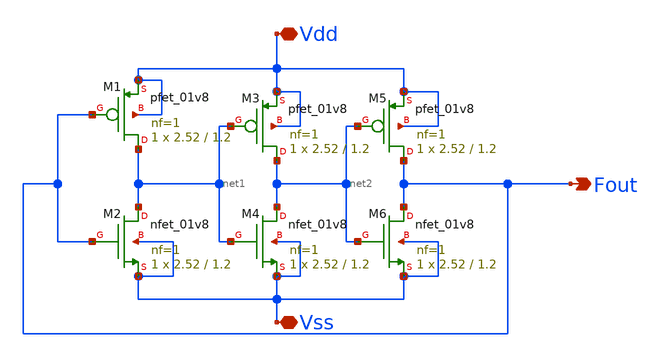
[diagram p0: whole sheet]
** sch_path: Week5/images/pre-layout_1bitADC/ring_osc.sch
**.subckt ring_osc Vdd Vss Fout
*.iopin Vdd
*.iopin Vss
*.opin Fout
XM1 net1 Fout Vdd Vdd sky130_fd_pr__pfet_01v8 L=1.2 W=2.52 nf=1 ad='int((nf+1)/2) * W/nf * 0.29' as='int((nf+2)/2) * W/nf * 0.29'
+ pd='2*int((nf+1)/2) * (W/nf + 0.29)' ps='2*int((nf+2)/2) * (W/nf + 0.29)' nrd='0.29 / W' nrs='0.29 / W'
+ sa=0 sb=0 sd=0 mult=1 m=1
XM2 net1 Fout Vss Vss sky130_fd_pr__nfet_01v8 L=1.2 W=2.52 nf=1 ad='int((nf+1)/2) * W/nf * 0.29' as='int((nf+2)/2) * W/nf * 0.29'
+ pd='2*int((nf+1)/2) * (W/nf + 0.29)' ps='2*int((nf+2)/2) * (W/nf + 0.29)' nrd='0.29 / W' nrs='0.29 / W'
+ sa=0 sb=0 sd=0 mult=1 m=1
XM3 net2 net1 Vdd Vdd sky130_fd_pr__pfet_01v8 L=1.2 W=2.52 nf=1 ad='int((nf+1)/2) * W/nf * 0.29' as='int((nf+2)/2) * W/nf * 0.29'
+ pd='2*int((nf+1)/2) * (W/nf + 0.29)' ps='2*int((nf+2)/2) * (W/nf + 0.29)' nrd='0.29 / W' nrs='0.29 / W'
+ sa=0 sb=0 sd=0 mult=1 m=1
XM4 net2 net1 Vss Vss sky130_fd_pr__nfet_01v8 L=1.2 W=2.52 nf=1 ad='int((nf+1)/2) * W/nf * 0.29' as='int((nf+2)/2) * W/nf * 0.29'
+ pd='2*int((nf+1)/2) * (W/nf + 0.29)' ps='2*int((nf+2)/2) * (W/nf + 0.29)' nrd='0.29 / W' nrs='0.29 / W'
+ sa=0 sb=0 sd=0 mult=1 m=1
XM5 Fout net2 Vdd Vdd sky130_fd_pr__pfet_01v8 L=1.2 W=2.52 nf=1 ad='int((nf+1)/2) * W/nf * 0.29' as='int((nf+2)/2) * W/nf * 0.29'
+ pd='2*int((nf+1)/2) * (W/nf + 0.29)' ps='2*int((nf+2)/2) * (W/nf + 0.29)' nrd='0.29 / W' nrs='0.29 / W'
+ sa=0 sb=0 sd=0 mult=1 m=1
XM6 Fout net2 Vss Vss sky130_fd_pr__nfet_01v8 L=1.2 W=2.52 nf=1 ad='int((nf+1)/2) * W/nf * 0.29' as='int((nf+2)/2) * W/nf * 0.29'
+ pd='2*int((nf+1)/2) * (W/nf + 0.29)' ps='2*int((nf+2)/2) * (W/nf + 0.29)' nrd='0.29 / W' nrs='0.29 / W'
+ sa=0 sb=0 sd=0 mult=1 m=1
**.ends
.end
